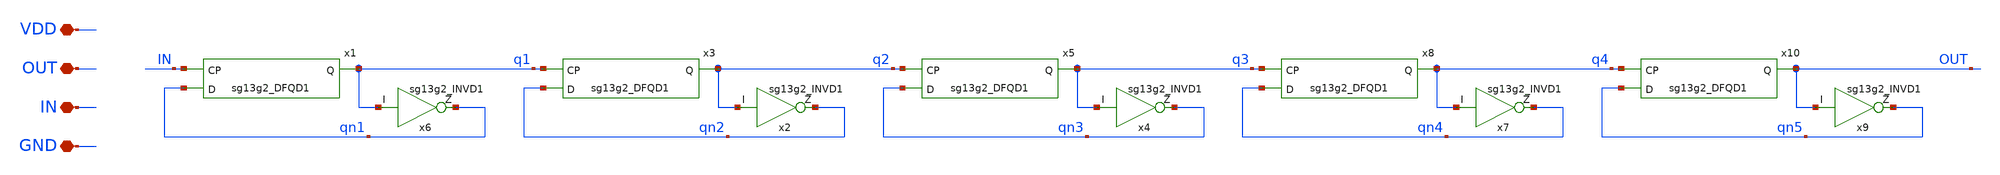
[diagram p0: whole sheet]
** sch_path: unic_cass_wrapper_user_project/ROs_reliability/div_sg13g2.sch
**.subckt div_sg13g2 GND IN VDD OUT
*.iopin GND
*.iopin IN
*.iopin VDD
*.iopin OUT
x6 q1 qn1 GND VDD sg13g2_INVD1
x1 IN qn1 q1 VDD GND sg13g2_DFQD1
x2 q2 qn2 GND VDD sg13g2_INVD1
x3 q1 qn2 q2 VDD GND sg13g2_DFQD1
x4 q3 qn3 GND VDD sg13g2_INVD1
x5 q2 qn3 q3 VDD GND sg13g2_DFQD1
x7 q4 qn4 GND VDD sg13g2_INVD1
x8 q3 qn4 q4 VDD GND sg13g2_DFQD1
x9 OUT qn5 GND VDD sg13g2_INVD1
x10 q4 qn5 OUT VDD GND sg13g2_DFQD1
**.ends
.end
